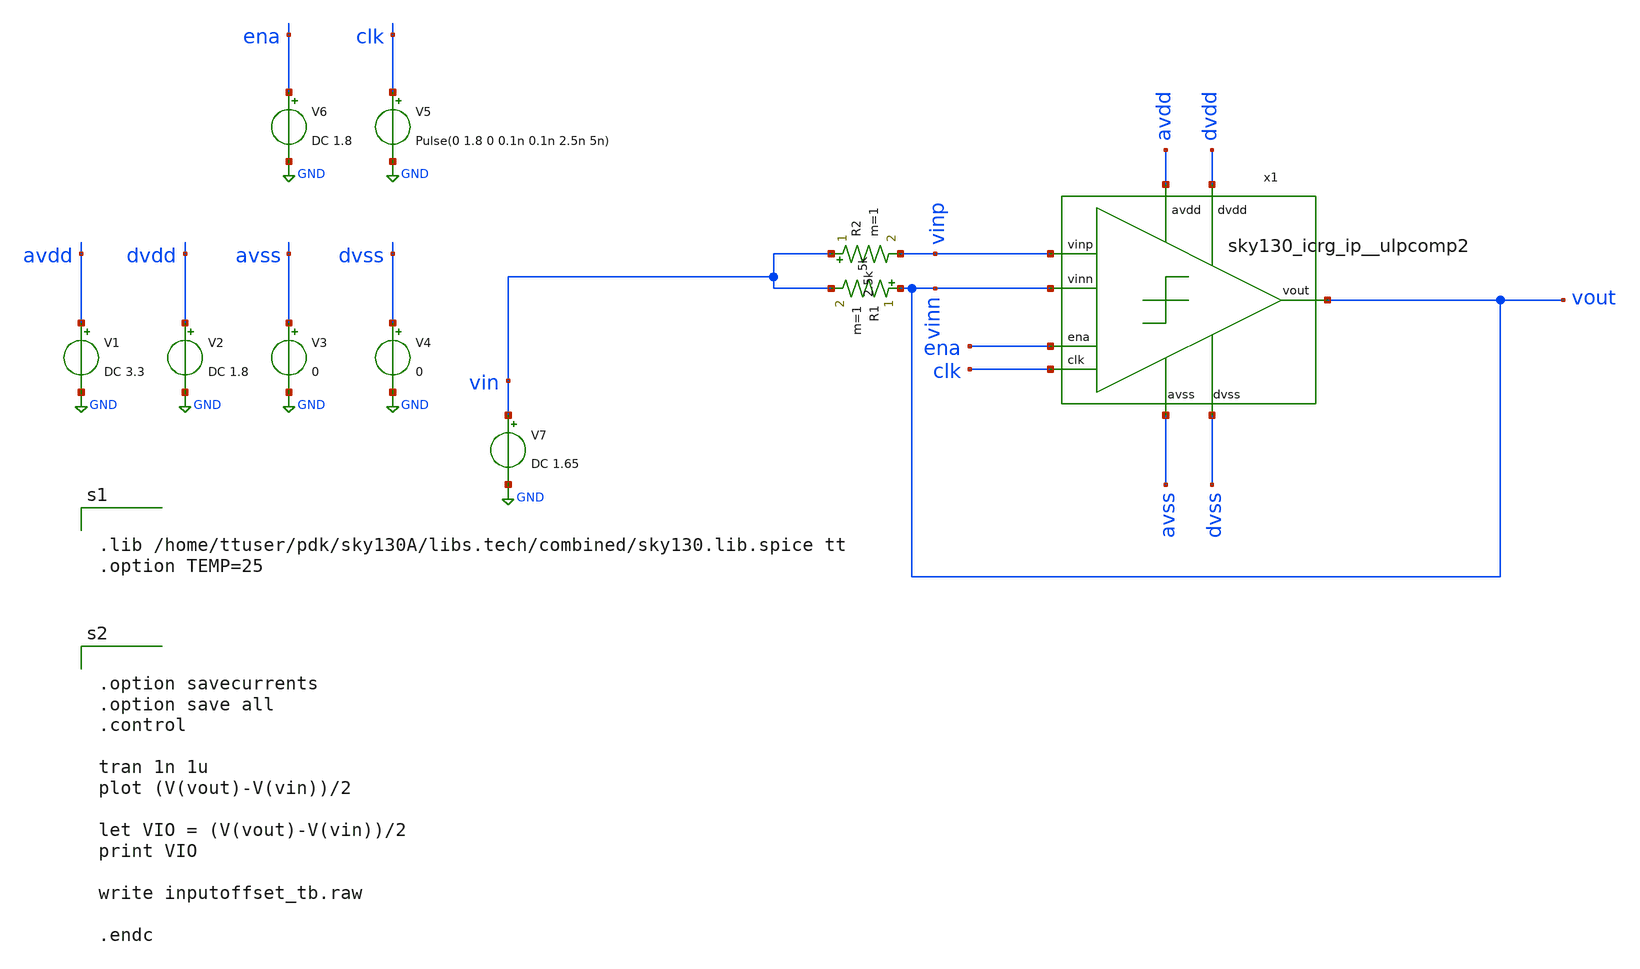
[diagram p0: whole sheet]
** sch_path: xschem/inputoffset_tb.sch
**.subckt inputoffset_tb
x1 dvdd avdd ena vinn vinn vinp clk dvss avss sky130_icrg_ip__ulpcomp2
V1 avdd GND DC 3.3
V2 dvdd GND DC 1.8
V3 avss GND 0
V4 dvss GND 0
V5 clk GND Pulse(0 1.8 0 0.1n 0.1n 2.5n 5n)
V6 ena GND DC 1.8
V7 vin GND DC 1.65
R1 vinn vin 5k m=1
R2 vin vinp 2.5k m=1
**** begin user architecture code


.lib /home/ttuser/pdk/sky130A/libs.tech/combined/sky130.lib.spice tt
.option TEMP=25



.option savecurrents
.option save all
.control

tran 1n 1u
plot (V(vout)-V(vin))/2

let VIO = (V(vout)-V(vin))/2
print VIO

write inputoffset_tb.raw

.endc

**** end user architecture code
**.ends

* expanding   symbol:  sky130_icrg_ip__ulpcomp2.sym # of pins=9
** sym_path: xschem/sky130_icrg_ip__ulpcomp2.sym
** sch_path: xschem/sky130_icrg_ip__ulpcomp2.sch
.subckt sky130_icrg_ip__ulpcomp2 dvdd avdd ena vout vinn vinp clk dvss avss
*.ipin avdd
*.ipin vinp
*.ipin vinn
*.opin avss
*.opin vout
*.opin dvss
*.ipin dvdd
*.ipin clk
*.ipin ena
x1 dvddb clka clk clkb dvss Stage0_clk_inv
x2 avdd enab clka vinn vinp net2 net1 avss Stage1
x3 dvdd enab dvddb clkb vout net2 net1 dvss Stage2_latch
x4 dvdd ena enab dvss Stage0_ena_inv
.ends


* expanding   symbol:  Stage0_clk_inv.sym # of pins=5
** sym_path: xschem/Stage0_clk_inv.sym
** sch_path: xschem/Stage0_clk_inv.sch
.subckt Stage0_clk_inv dvddb clka clk clkb dvss
*.opin dvss
*.ipin dvddb
*.opin clka
*.ipin clk
*.opin clkb
XM22 clka clkb dvddb dvddb sky130_fd_pr__pfet_01v8 L=0.5 W=2 nf=1 ad='int((nf+1)/2) * W/nf * 0.29' as='int((nf+2)/2) * W/nf * 0.29'
+ pd='2*int((nf+1)/2) * (W/nf + 0.29)' ps='2*int((nf+2)/2) * (W/nf + 0.29)' nrd='0.29 / W' nrs='0.29 / W'
+ sa=0 sb=0 sd=0 mult=1 m=1
XM8 clkb clk dvddb dvddb sky130_fd_pr__pfet_01v8 L=0.5 W=2 nf=1 ad='int((nf+1)/2) * W/nf * 0.29' as='int((nf+2)/2) * W/nf * 0.29'
+ pd='2*int((nf+1)/2) * (W/nf + 0.29)' ps='2*int((nf+2)/2) * (W/nf + 0.29)' nrd='0.29 / W' nrs='0.29 / W'
+ sa=0 sb=0 sd=0 mult=1 m=1
XM6 clkb clk dvss dvss sky130_fd_pr__nfet_01v8 L=0.5 W=1 nf=1 ad='int((nf+1)/2) * W/nf * 0.29' as='int((nf+2)/2) * W/nf * 0.29'
+ pd='2*int((nf+1)/2) * (W/nf + 0.29)' ps='2*int((nf+2)/2) * (W/nf + 0.29)' nrd='0.29 / W' nrs='0.29 / W'
+ sa=0 sb=0 sd=0 mult=1 m=1
XM21 clka clkb dvss dvss sky130_fd_pr__nfet_01v8 L=0.5 W=1 nf=1 ad='int((nf+1)/2) * W/nf * 0.29' as='int((nf+2)/2) * W/nf * 0.29'
+ pd='2*int((nf+1)/2) * (W/nf + 0.29)' ps='2*int((nf+2)/2) * (W/nf + 0.29)' nrd='0.29 / W' nrs='0.29 / W'
+ sa=0 sb=0 sd=0 mult=1 m=1
.ends


* expanding   symbol:  Stage1.sym # of pins=8
** sym_path: xschem/Stage1.sym
** sch_path: xschem/Stage1.sch
.subckt Stage1 avdd enab clka vinn vinp oneg opos avss
*.ipin avdd
*.ipin vinp
*.ipin vinn
*.opin avss
*.ipin clka
*.opin opos
*.opin oneg
*.ipin enab
XM2 oneg vinp net1 net1 sky130_fd_pr__pfet_g5v0d10v5 L=1 W=5 nf=1 ad='int((nf+1)/2) * W/nf * 0.29' as='int((nf+2)/2) * W/nf * 0.29'
+ pd='2*int((nf+1)/2) * (W/nf + 0.29)' ps='2*int((nf+2)/2) * (W/nf + 0.29)' nrd='0.29 / W' nrs='0.29 / W'
+ sa=0 sb=0 sd=0 mult=1 m=1
XM3 opos vinn net1 net1 sky130_fd_pr__pfet_g5v0d10v5 L=1 W=5 nf=1 ad='int((nf+1)/2) * W/nf * 0.29' as='int((nf+2)/2) * W/nf * 0.29'
+ pd='2*int((nf+1)/2) * (W/nf + 0.29)' ps='2*int((nf+2)/2) * (W/nf + 0.29)' nrd='0.29 / W' nrs='0.29 / W'
+ sa=0 sb=0 sd=0 mult=1 m=1
XM7 oneg clka net2 net2 sky130_fd_pr__nfet_03v3_nvt L=0.5 W=3 nf=1 ad='int((nf+1)/2) * W/nf * 0.29' as='int((nf+2)/2) * W/nf * 0.29'
+ pd='2*int((nf+1)/2) * (W/nf + 0.29)' ps='2*int((nf+2)/2) * (W/nf + 0.29)' nrd='0.29 / W' nrs='0.29 / W'
+ sa=0 sb=0 sd=0 mult=1 m=1
XM5 opos clka net2 net2 sky130_fd_pr__nfet_03v3_nvt L=0.5 W=3 nf=1 ad='int((nf+1)/2) * W/nf * 0.29' as='int((nf+2)/2) * W/nf * 0.29'
+ pd='2*int((nf+1)/2) * (W/nf + 0.29)' ps='2*int((nf+2)/2) * (W/nf + 0.29)' nrd='0.29 / W' nrs='0.29 / W'
+ sa=0 sb=0 sd=0 mult=1 m=1
XM4 net2 net2 avss avss sky130_fd_pr__nfet_03v3_nvt L=0.5 W=3 nf=1 ad='int((nf+1)/2) * W/nf * 0.29' as='int((nf+2)/2) * W/nf * 0.29'
+ pd='2*int((nf+1)/2) * (W/nf + 0.29)' ps='2*int((nf+2)/2) * (W/nf + 0.29)' nrd='0.29 / W' nrs='0.29 / W'
+ sa=0 sb=0 sd=0 mult=1 m=1
XM20 net3 enab avdd avdd sky130_fd_pr__pfet_g5v0d10v5 L=1 W=5 nf=1 ad='int((nf+1)/2) * W/nf * 0.29' as='int((nf+2)/2) * W/nf * 0.29'
+ pd='2*int((nf+1)/2) * (W/nf + 0.29)' ps='2*int((nf+2)/2) * (W/nf + 0.29)' nrd='0.29 / W' nrs='0.29 / W'
+ sa=0 sb=0 sd=0 mult=1 m=1
XM1 net1 clka net3 net3 sky130_fd_pr__pfet_g5v0d10v5 L=1 W=5 nf=1 ad='int((nf+1)/2) * W/nf * 0.29' as='int((nf+2)/2) * W/nf * 0.29'
+ pd='2*int((nf+1)/2) * (W/nf + 0.29)' ps='2*int((nf+2)/2) * (W/nf + 0.29)' nrd='0.29 / W' nrs='0.29 / W'
+ sa=0 sb=0 sd=0 mult=1 m=1
.ends


* expanding   symbol:  Stage2_latch.sym # of pins=8
** sym_path: xschem/Stage2_latch.sym
** sch_path: xschem/Stage2_latch.sch
.subckt Stage2_latch dvdd enab dvddb clkb vout oneg opos dvss
*.ipin clkb
*.opin vout
*.opin dvss
*.ipin dvdd
*.ipin opos
*.ipin oneg
*.ipin enab
*.opin dvddb
XM18 vout net1 dvss dvss sky130_fd_pr__nfet_01v8 L=0.5 W=1 nf=1 ad='int((nf+1)/2) * W/nf * 0.29' as='int((nf+2)/2) * W/nf * 0.29'
+ pd='2*int((nf+1)/2) * (W/nf + 0.29)' ps='2*int((nf+2)/2) * (W/nf + 0.29)' nrd='0.29 / W' nrs='0.29 / W'
+ sa=0 sb=0 sd=0 mult=1 m=1
XM19 vout net1 dvddb dvddb sky130_fd_pr__pfet_01v8 L=1 W=2 nf=1 ad='int((nf+1)/2) * W/nf * 0.29' as='int((nf+2)/2) * W/nf * 0.29'
+ pd='2*int((nf+1)/2) * (W/nf + 0.29)' ps='2*int((nf+2)/2) * (W/nf + 0.29)' nrd='0.29 / W' nrs='0.29 / W'
+ sa=0 sb=0 sd=0 mult=1 m=1
XM13 net1 opos net3 dvss sky130_fd_pr__nfet_03v3_nvt L=0.5 W=2 nf=1 ad='int((nf+1)/2) * W/nf * 0.29'
+ as='int((nf+2)/2) * W/nf * 0.29' pd='2*int((nf+1)/2) * (W/nf + 0.29)' ps='2*int((nf+2)/2) * (W/nf + 0.29)'
+ nrd='0.29 / W' nrs='0.29 / W' sa=0 sb=0 sd=0 mult=1 m=1
XM14 net4 net1 net5 dvss sky130_fd_pr__nfet_03v3_nvt L=0.5 W=2 nf=1 ad='int((nf+1)/2) * W/nf * 0.29'
+ as='int((nf+2)/2) * W/nf * 0.29' pd='2*int((nf+1)/2) * (W/nf + 0.29)' ps='2*int((nf+2)/2) * (W/nf + 0.29)'
+ nrd='0.29 / W' nrs='0.29 / W' sa=0 sb=0 sd=0 mult=1 m=1
XM15 net5 clkb dvss dvss sky130_fd_pr__nfet_03v3_nvt L=0.5 W=2 nf=1 ad='int((nf+1)/2) * W/nf * 0.29'
+ as='int((nf+2)/2) * W/nf * 0.29' pd='2*int((nf+1)/2) * (W/nf + 0.29)' ps='2*int((nf+2)/2) * (W/nf + 0.29)'
+ nrd='0.29 / W' nrs='0.29 / W' sa=0 sb=0 sd=0 mult=1 m=1
XM16 net3 net2 net5 dvss sky130_fd_pr__nfet_03v3_nvt L=0.5 W=2 nf=1 ad='int((nf+1)/2) * W/nf * 0.29'
+ as='int((nf+2)/2) * W/nf * 0.29' pd='2*int((nf+1)/2) * (W/nf + 0.29)' ps='2*int((nf+2)/2) * (W/nf + 0.29)'
+ nrd='0.29 / W' nrs='0.29 / W' sa=0 sb=0 sd=0 mult=1 m=1
XM17 net2 oneg net4 dvss sky130_fd_pr__nfet_03v3_nvt L=0.5 W=2 nf=1 ad='int((nf+1)/2) * W/nf * 0.29'
+ as='int((nf+2)/2) * W/nf * 0.29' pd='2*int((nf+1)/2) * (W/nf + 0.29)' ps='2*int((nf+2)/2) * (W/nf + 0.29)'
+ nrd='0.29 / W' nrs='0.29 / W' sa=0 sb=0 sd=0 mult=1 m=1
XM23 dvddb enab dvdd dvdd sky130_fd_pr__pfet_01v8_hvt L=0.15 W=1 nf=1 ad='int((nf+1)/2) * W/nf * 0.29'
+ as='int((nf+2)/2) * W/nf * 0.29' pd='2*int((nf+1)/2) * (W/nf + 0.29)' ps='2*int((nf+2)/2) * (W/nf + 0.29)'
+ nrd='0.29 / W' nrs='0.29 / W' sa=0 sb=0 sd=0 mult=1 m=1
XM9 net1 clkb dvddb dvddb sky130_fd_pr__pfet_01v8_hvt L=1 W=3 nf=1 ad='int((nf+1)/2) * W/nf * 0.29' as='int((nf+2)/2) * W/nf * 0.29'
+ pd='2*int((nf+1)/2) * (W/nf + 0.29)' ps='2*int((nf+2)/2) * (W/nf + 0.29)' nrd='0.29 / W' nrs='0.29 / W'
+ sa=0 sb=0 sd=0 mult=2 m=2
XM10 net2 net1 dvddb dvddb sky130_fd_pr__pfet_01v8_hvt L=1 W=3 nf=1 ad='int((nf+1)/2) * W/nf * 0.29'
+ as='int((nf+2)/2) * W/nf * 0.29' pd='2*int((nf+1)/2) * (W/nf + 0.29)' ps='2*int((nf+2)/2) * (W/nf + 0.29)'
+ nrd='0.29 / W' nrs='0.29 / W' sa=0 sb=0 sd=0 mult=2 m=2
XM11 net1 net2 dvddb dvddb sky130_fd_pr__pfet_01v8_hvt L=1 W=3 nf=1 ad='int((nf+1)/2) * W/nf * 0.29'
+ as='int((nf+2)/2) * W/nf * 0.29' pd='2*int((nf+1)/2) * (W/nf + 0.29)' ps='2*int((nf+2)/2) * (W/nf + 0.29)'
+ nrd='0.29 / W' nrs='0.29 / W' sa=0 sb=0 sd=0 mult=2 m=2
XM12 net2 clkb dvddb dvddb sky130_fd_pr__pfet_01v8_hvt L=1 W=3 nf=1 ad='int((nf+1)/2) * W/nf * 0.29'
+ as='int((nf+2)/2) * W/nf * 0.29' pd='2*int((nf+1)/2) * (W/nf + 0.29)' ps='2*int((nf+2)/2) * (W/nf + 0.29)'
+ nrd='0.29 / W' nrs='0.29 / W' sa=0 sb=0 sd=0 mult=2 m=2
.ends


* expanding   symbol:  Stage0_ena_inv.sym # of pins=4
** sym_path: xschem/Stage0_ena_inv.sym
** sch_path: xschem/Stage0_ena_inv.sch
.subckt Stage0_ena_inv dvdd ena enab dvss
*.ipin ena
*.ipin dvdd
*.opin dvss
*.opin enab
XM25 enab ena dvdd dvdd sky130_fd_pr__pfet_01v8 L=0.5 W=2 nf=1 ad='int((nf+1)/2) * W/nf * 0.29' as='int((nf+2)/2) * W/nf * 0.29'
+ pd='2*int((nf+1)/2) * (W/nf + 0.29)' ps='2*int((nf+2)/2) * (W/nf + 0.29)' nrd='0.29 / W' nrs='0.29 / W'
+ sa=0 sb=0 sd=0 mult=1 m=1
XM24 enab ena dvss dvss sky130_fd_pr__nfet_01v8 L=0.5 W=1 nf=1 ad='int((nf+1)/2) * W/nf * 0.29' as='int((nf+2)/2) * W/nf * 0.29'
+ pd='2*int((nf+1)/2) * (W/nf + 0.29)' ps='2*int((nf+2)/2) * (W/nf + 0.29)' nrd='0.29 / W' nrs='0.29 / W'
+ sa=0 sb=0 sd=0 mult=1 m=1
.ends

.GLOBAL GND
.end
